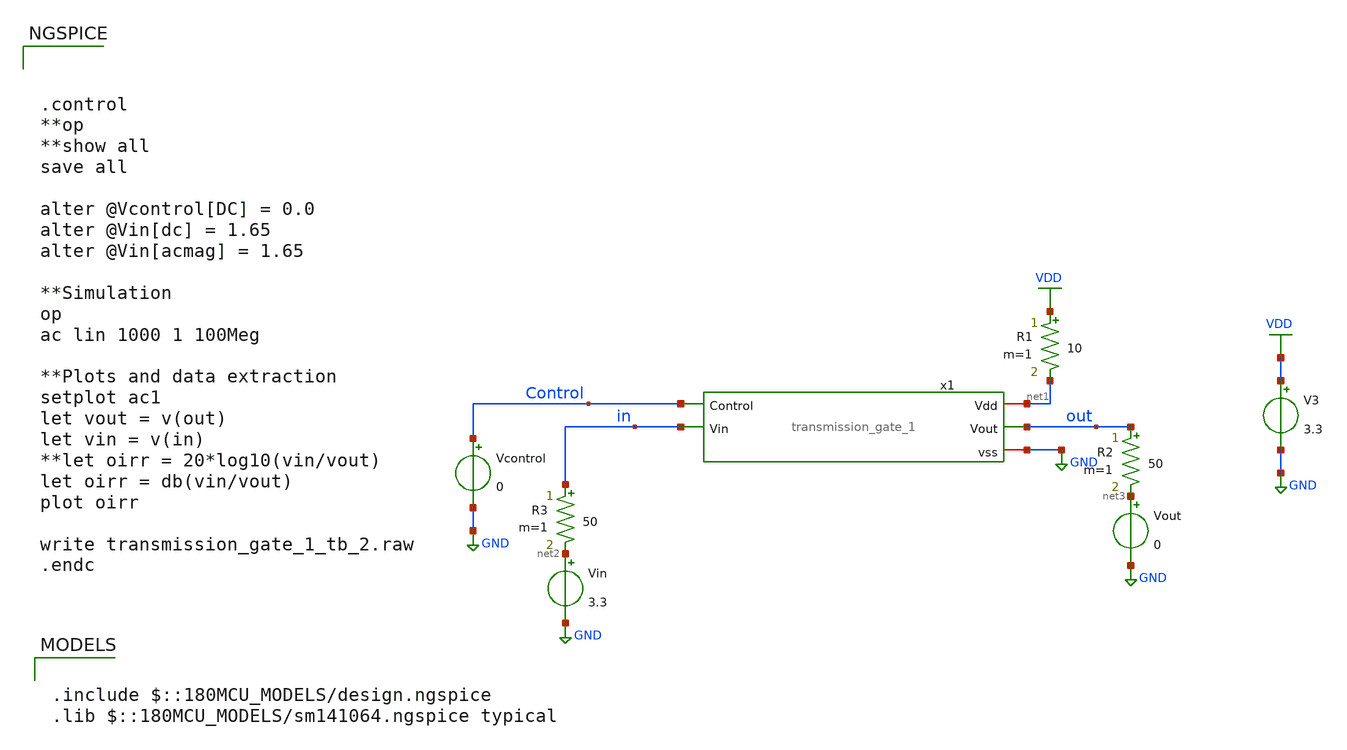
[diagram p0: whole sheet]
** sch_path: designs/libs/core_analog/Transmission_Gate/transmission_gate_1_tb_2.sch
**.subckt transmission_gate_1_tb_2
x1 net1 Control out in GND transmission_gate_1
Vin net2 GND 3.3
Vcontrol Control GND 0
V3 VDD GND 3.3
Vout net3 GND 0
R1 VDD net1 10 m=1
R2 out net3 50 m=1
R3 in net2 50 m=1
**** begin user architecture code

.include $::180MCU_MODELS/design.ngspice
.lib $::180MCU_MODELS/sm141064.ngspice typical




.control
**op
**show all
save all

alter @Vcontrol[DC] = 0.0
alter @Vin[dc] = 1.65
alter @Vin[acmag] = 1.65

**Simulation
op
ac lin 1000 1 100Meg

**Plots and data extraction
setplot ac1
let vout = v(out)
let vin = v(in)
**let oirr = 20*log10(vin/vout)
let oirr = db(vin/vout)
plot oirr

write transmission_gate_1_tb_2.raw
.endc


**** end user architecture code
**.ends

* expanding   symbol:  transmission_gate_1.sym # of pins=5
** sym_path: designs/libs/core_analog/Transmission_Gate/transmission_gate_1.sym
** sch_path: designs/libs/core_analog/Transmission_Gate/transmission_gate_1.sch
.subckt transmission_gate_1 Vdd Control Vout Vin vss
*.iopin Vdd
*.ipin Control
*.opin Vout
*.ipin Vin
*.iopin vss
XM1 net1 Control vss vss nfet_03v3 L=0.28u W=0.85u nf=1 ad='int((nf+1)/2) * W/nf * 0.18u' as='int((nf+2)/2) * W/nf * 0.18u'
+ pd='2*int((nf+1)/2) * (W/nf + 0.18u)' ps='2*int((nf+2)/2) * (W/nf + 0.18u)' nrd='0.18u / W' nrs='0.18u / W'
+ sa=0 sb=0 sd=0 m=1
XM2 net1 Control Vdd Vdd pfet_03v3 L=0.28u W=1.7u nf=1 ad='int((nf+1)/2) * W/nf * 0.18u' as='int((nf+2)/2) * W/nf * 0.18u'
+ pd='2*int((nf+1)/2) * (W/nf + 0.18u)' ps='2*int((nf+2)/2) * (W/nf + 0.18u)' nrd='0.18u / W' nrs='0.18u / W'
+ sa=0 sb=0 sd=0 m=1
XM3 Vout Control Vin vss nfet_03v3 L=0.28u W=2.4u nf=1 ad='int((nf+1)/2) * W/nf * 0.18u' as='int((nf+2)/2) * W/nf * 0.18u'
+ pd='2*int((nf+1)/2) * (W/nf + 0.18u)' ps='2*int((nf+2)/2) * (W/nf + 0.18u)' nrd='0.18u / W' nrs='0.18u / W'
+ sa=0 sb=0 sd=0 m=10
XM4 Vout net1 Vin Vdd pfet_03v3 L=0.28u W=7.2u nf=1 ad='int((nf+1)/2) * W/nf * 0.18u' as='int((nf+2)/2) * W/nf * 0.18u'
+ pd='2*int((nf+1)/2) * (W/nf + 0.18u)' ps='2*int((nf+2)/2) * (W/nf + 0.18u)' nrd='0.18u / W' nrs='0.18u / W'
+ sa=0 sb=0 sd=0 m=10
.ends

.GLOBAL VDD
.GLOBAL GND
.end
